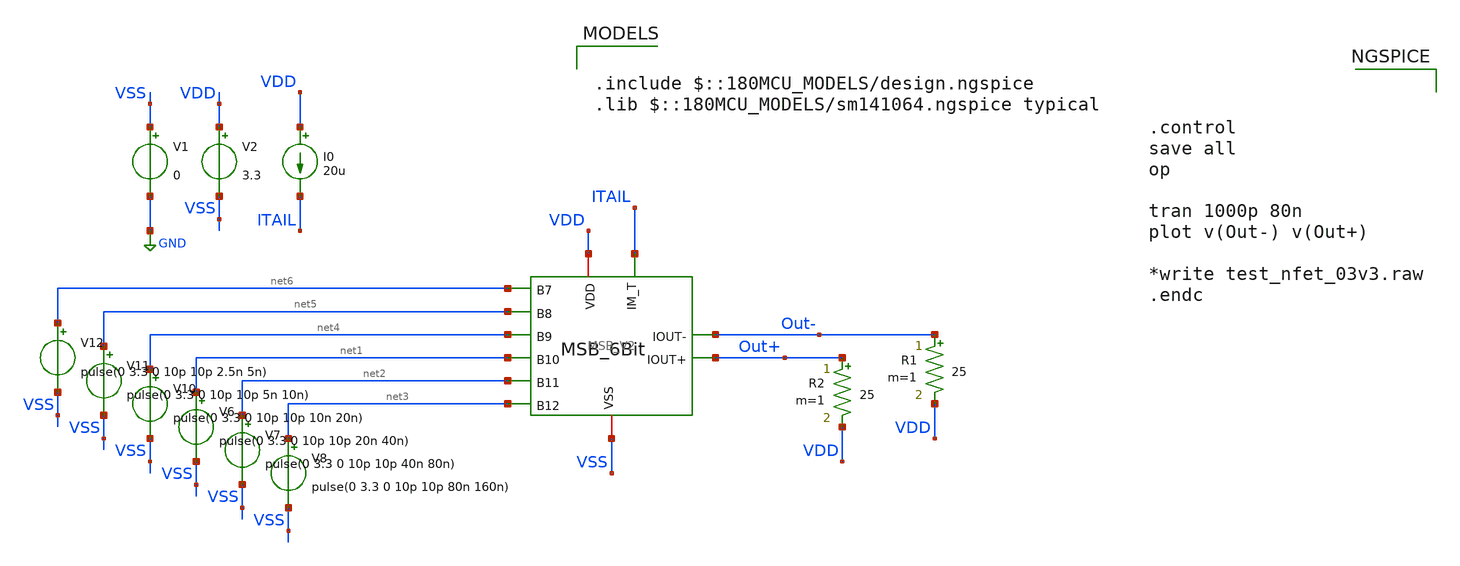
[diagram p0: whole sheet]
** sch_path: DAC_PAKISTAN_01/Pakistan1_Xschem/MSB_TB.sch
**.subckt MSB_TB
V1 VSS GND 0
V2 VDD VSS 3.3
V6 net1 VSS pulse(0 3.3 0 10p 10p 20n 40n)
V7 net2 VSS pulse(0 3.3 0 10p 10p 40n 80n)
V8 net3 VSS pulse(0 3.3 0 10p 10p 80n 160n)
V10 net4 VSS pulse(0 3.3 0 10p 10p 10n 20n)
V11 net5 VSS pulse(0 3.3 0 10p 10p 5n 10n)
V12 net6 VSS pulse(0 3.3 0 10p 10p 2.5n 5n)
R1 Out- VDD 25 m=1
R2 Out+ VDD 25 m=1
I0 VDD ITAIL 20u
x1 VSS VDD net2 net6 net5 net3 net4 ITAIL net1 Out- Out+ MSB_V2
**** begin user architecture code

.include $::180MCU_MODELS/design.ngspice
.lib $::180MCU_MODELS/sm141064.ngspice typical




.control
save all
op

tran 1000p 80n
plot v(Out-) v(Out+)

*write test_nfet_03v3.raw
.endc


**** end user architecture code
**.ends
.GLOBAL GND
.end
